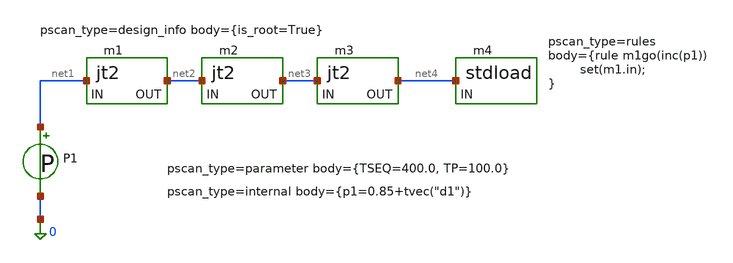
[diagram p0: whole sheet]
** sch_path: examples/jt2tb/jt2tb.sch
**.subckt jt2tb
Xm1 net1 net2 jt2
P1 net1 0 P1
Xm2 net2 net3 jt2
Xm3 net3 net4 jt2
Xm4 net4 stdload
**.ends

* expanding   symbol:  jt2.sym # of pins=2
** sym_path: cells/jt2.sym
** sch_path: cells/jt2.sch
.subckt jt2 IN OUT
*.iopin OUT
*.iopin IN
L1 net3 net2 0.75 m=1
L2 net2 net1 0.75 m=1
I0 0 net2 I?
L5 net1 IN 0.75 m=1
L6 OUT net3 0.75 m=1
J1 net1 0 J
J2 net3 0 J
.ends


* expanding   symbol:  stdload.sym # of pins=1
** sym_path: cells/stdload.sym
** sch_path: cells/stdload.sch
.subckt stdload IN
*.iopin IN
Xm1 IN net1 jt2
R1 net2 0 0.5 m=1
Xm2 net1 net2 jt2
.ends

.end
